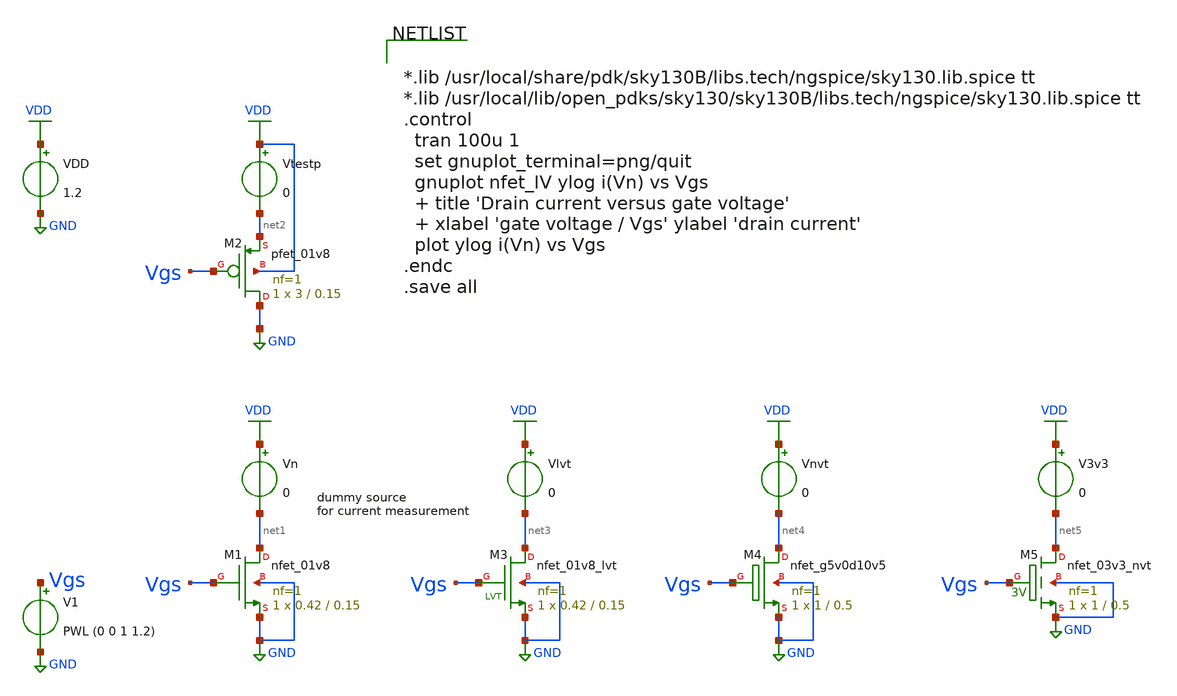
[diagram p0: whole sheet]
** sch_path: xschem/test_bench/nfet_IV_tb.sch
**.subckt nfet_IV_tb
XM1 net1 Vgs GND GND sky130_fd_pr__nfet_01v8 L=0.15 W=0.42 nf=1 ad='int((nf+1)/2) * W/nf * 0.29' as='int((nf+2)/2) * W/nf * 0.29'
+ pd='2*int((nf+1)/2) * (W/nf + 0.29)' ps='2*int((nf+2)/2) * (W/nf + 0.29)' nrd='0.29 / W' nrs='0.29 / W'
+ sa=0 sb=0 sd=0 mult=1 m=1
V1 Vgs GND PWL (0 0 1 1.2)
VDD VDD GND 1.2
Vn VDD net1 0
Vtestp VDD net2 0
XM2 GND Vgs net2 VDD sky130_fd_pr__pfet_01v8 L=0.15 W=3 nf=1 ad='int((nf+1)/2) * W/nf * 0.29' as='int((nf+2)/2) * W/nf * 0.29'
+ pd='2*int((nf+1)/2) * (W/nf + 0.29)' ps='2*int((nf+2)/2) * (W/nf + 0.29)' nrd='0.29 / W' nrs='0.29 / W'
+ sa=0 sb=0 sd=0 mult=1 m=1
Vlvt VDD net3 0
Vnvt VDD net4 0
XM3 net3 Vgs GND GND sky130_fd_pr__nfet_01v8_lvt L=0.15 W=0.42 nf=1 ad='int((nf+1)/2) * W/nf * 0.29'
+ as='int((nf+2)/2) * W/nf * 0.29' pd='2*int((nf+1)/2) * (W/nf + 0.29)' ps='2*int((nf+2)/2) * (W/nf + 0.29)'
+ nrd='0.29 / W' nrs='0.29 / W' sa=0 sb=0 sd=0 mult=1 m=1
XM4 net4 Vgs GND GND sky130_fd_pr__nfet_g5v0d10v5 L=0.5 W=1 nf=1 ad='int((nf+1)/2) * W/nf * 0.29' as='int((nf+2)/2) * W/nf * 0.29'
+ pd='2*int((nf+1)/2) * (W/nf + 0.29)' ps='2*int((nf+2)/2) * (W/nf + 0.29)' nrd='0.29 / W' nrs='0.29 / W'
+ sa=0 sb=0 sd=0 mult=1 m=1
V3v3 VDD net5 0
XM5 net5 Vgs GND GND sky130_fd_pr__nfet_03v3_nvt L=0.5 W=1 nf=1 ad='int((nf+1)/2) * W/nf * 0.29' as='int((nf+2)/2) * W/nf * 0.29'
+ pd='2*int((nf+1)/2) * (W/nf + 0.29)' ps='2*int((nf+2)/2) * (W/nf + 0.29)' nrd='0.29 / W' nrs='0.29 / W'
+ sa=0 sb=0 sd=0 mult=1 m=1
**** begin user architecture code


*.lib /usr/local/share/pdk/sky130B/libs.tech/ngspice/sky130.lib.spice tt
*.lib /usr/local/lib/open_pdks/sky130/sky130B/libs.tech/ngspice/sky130.lib.spice tt
.control
  tran 100u 1
  set gnuplot_terminal=png/quit
  gnuplot nfet_IV ylog i(Vn) vs Vgs
  + title 'Drain current versus gate voltage'
  + xlabel 'gate voltage / Vgs' ylabel 'drain current'
  plot ylog i(Vn) vs Vgs
.endc
.save all


 .lib $::SKYWATER_MODELS/sky130.lib.spice tt
.include $::SKYWATER_STDCELLS/sky130_fd_sc_hd.spice

**** end user architecture code
**.ends
.GLOBAL VDD
.GLOBAL GND
.end
